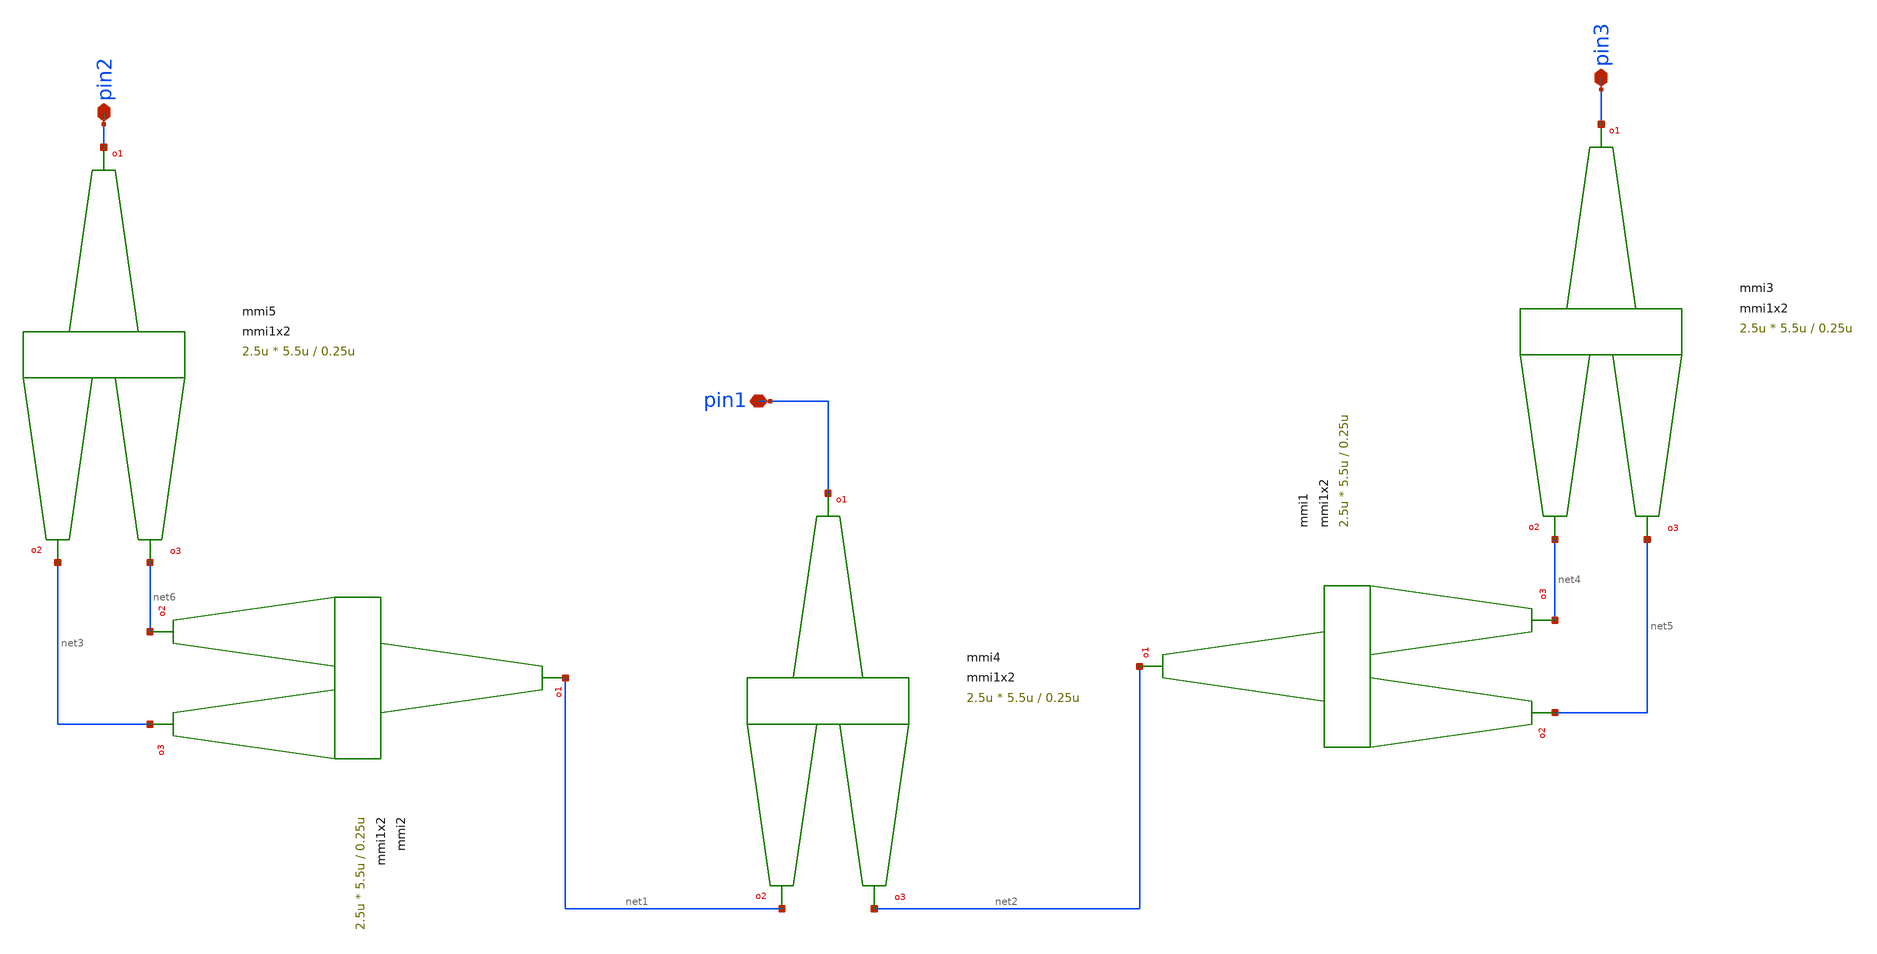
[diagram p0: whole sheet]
** sch_path: xschem/tests/test_sch/test_mmi1x2.sch
* Copyright (c) 2024, Mabrains LLC
* Licensed under the GNU Lesser General Public License, Version 3.0 (the "License");
* you may not use this file except in compliance with the License.
* GNU Lesser General Public License
* Version 3, 29 June 2007
* This program is free software: you can redistribute it and/or modify
* it under the terms of the GNU Lesser General Public License as published
* by the Free Software Foundation, either version 3 of the License, or
* (at your option) any later version.
* This program is distributed in the hope that it will be useful,
* but WITHOUT ANY WARRANTY; without even the implied warranty of
* MERCHANTABILITY or FITNESS FOR A PARTICULAR PURPOSE.  See the
* GNU Lesser General Public License for more details.
* You should have received a copy of the GNU Lesser General Public License
* along with this program.  If not, see <https://www.gnu.org/licenses/>.
* SPDX-License-Identifier: LGPL-3.0
**.subckt test_mmi1x2 pin1 pin3 pin2
*.iopin pin1
*.iopin pin3
*.iopin pin2
Pmmi4 pin1 net1 net2 mmi1x2 width=0.5u width_taper=1u length_taper=10u length_mmi=5.5u
+ width_mmi=2.5u gap_mmi=0.25u
Pmmi1 net2 net5 net4 mmi1x2 width=0.5u width_taper=1u length_taper=10u length_mmi=5.5u
+ width_mmi=2.5u gap_mmi=0.25u
Pmmi2 net1 net6 net3 mmi1x2 width=0.5u width_taper=1u length_taper=10u length_mmi=5.5u
+ width_mmi=2.5u gap_mmi=0.25u
Pmmi5 pin2 net3 net6 mmi1x2 width=0.5u width_taper=1u length_taper=10u length_mmi=5.5u
+ width_mmi=2.5u gap_mmi=0.25u
Pmmi3 pin3 net4 net5 mmi1x2 width=0.5u width_taper=1u length_taper=10u length_mmi=5.5u
+ width_mmi=2.5u gap_mmi=0.25u
**.ends
.end
